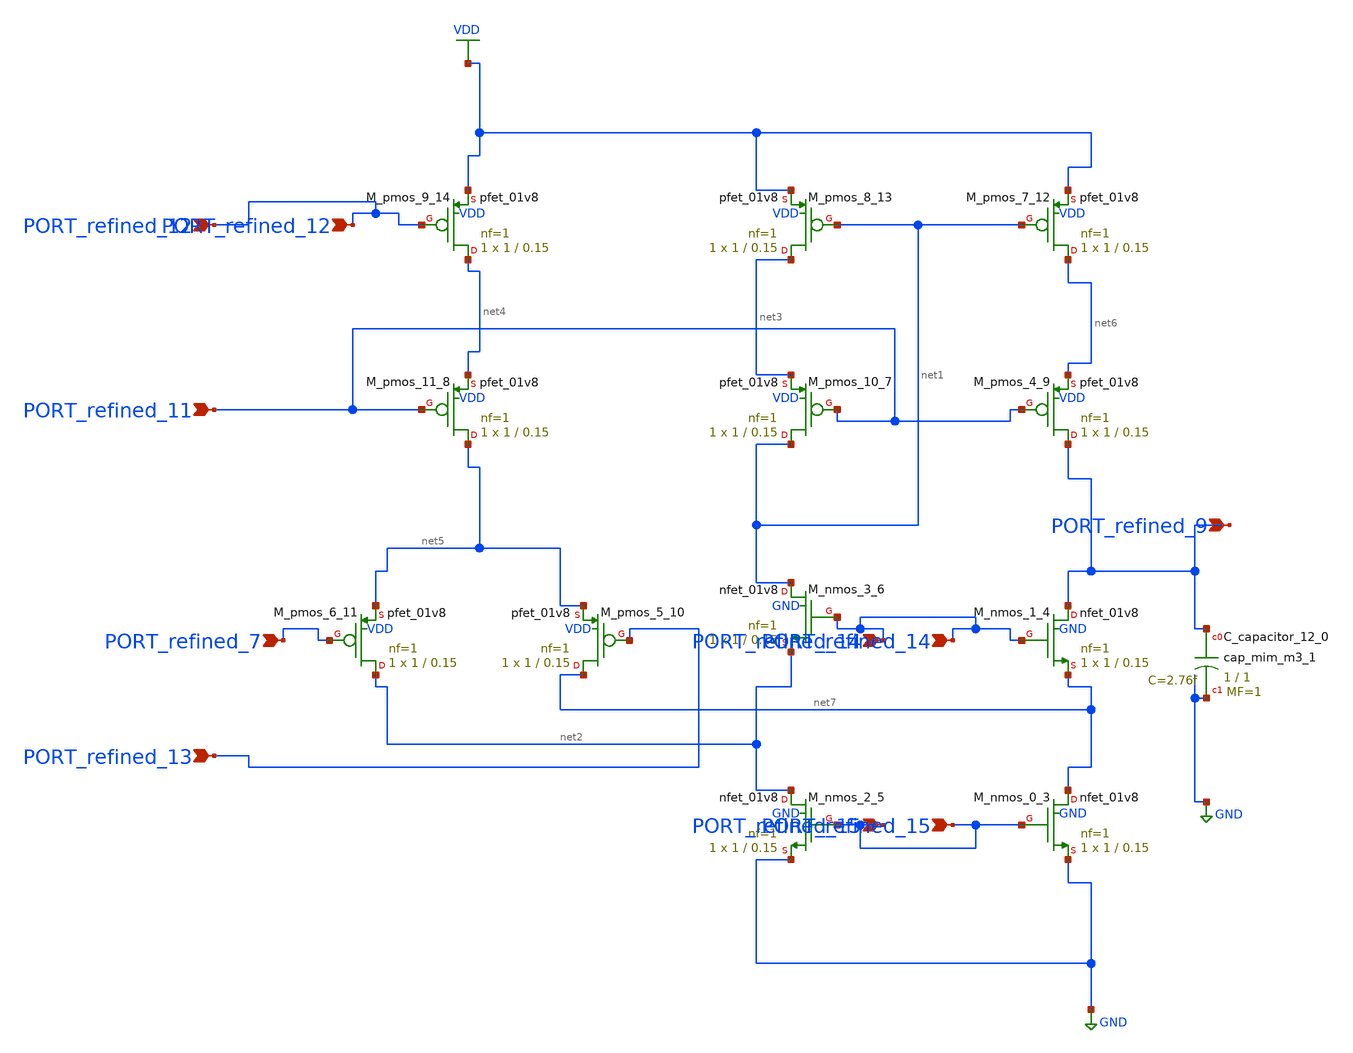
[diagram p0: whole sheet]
** sch_path: schematics/10_24425_ijet_2020_131876_02_002.sch
**.subckt 10_24425_ijet_2020_131876_02_002 PORT_refined_13 PORT_refined_9 PORT_refined_12
*+ PORT_refined_11 PORT_refined_15 PORT_refined_14 PORT_refined_15 PORT_refined_7 PORT_refined_14 PORT_refined_12
*.ipin PORT_refined_13
*.ipin PORT_refined_9
*.ipin PORT_refined_12
*.ipin PORT_refined_11
*.ipin PORT_refined_15
*.ipin PORT_refined_14
*.ipin PORT_refined_15
*.ipin PORT_refined_7
*.ipin PORT_refined_14
*.ipin PORT_refined_12
XC_capacitor_12_0 PORT_refined_9 GND sky130_fd_pr__cap_mim_m3_1 W=1 L=1 MF=1 m=1
XM_nmos_0_3 net7 PORT_refined_15 GND GND sky130_fd_pr__nfet_01v8 L=0.15 W=1 nf=1 ad='int((1 + 1)/2) * 1 / 1 * 0.29'
+ as='int((1 + 2)/2) * 1 / 1 * 0.29' pd='2*int((1 + 1)/2) * (1 / 1 + 0.29)' ps='2*int((1 + 2)/2) * (1 / 1 + 0.29)'
+ nrd='0.29 / 1 ' nrs='0.29 / 1 ' sa=0 sb=0 sd=0 mult=1 m=1
XM_nmos_1_4 PORT_refined_9 PORT_refined_14 net7 GND sky130_fd_pr__nfet_01v8 L=0.15 W=1 nf=1 ad='int((1 + 1)/2) * 1 / 1 * 0.29'
+ as='int((1 + 2)/2) * 1 / 1 * 0.29' pd='2*int((1 + 1)/2) * (1 / 1 + 0.29)' ps='2*int((1 + 2)/2) * (1 / 1 + 0.29)'
+ nrd='0.29 / 1 ' nrs='0.29 / 1 ' sa=0 sb=0 sd=0 mult=1 m=1
XM_nmos_2_5 net2 PORT_refined_15 GND GND sky130_fd_pr__nfet_01v8 L=0.15 W=1 nf=1 ad='int((1 + 1)/2) * 1 / 1 * 0.29'
+ as='int((1 + 2)/2) * 1 / 1 * 0.29' pd='2*int((1 + 1)/2) * (1 / 1 + 0.29)' ps='2*int((1 + 2)/2) * (1 / 1 + 0.29)'
+ nrd='0.29 / 1 ' nrs='0.29 / 1 ' sa=0 sb=0 sd=0 mult=1 m=1
XM_nmos_3_6 net1 PORT_refined_14 net2 GND sky130_fd_pr__nfet_01v8 L=0.15 W=1 nf=1 ad='int((1 + 1)/2) * 1 / 1 * 0.29'
+ as='int((1 + 2)/2) * 1 / 1 * 0.29' pd='2*int((1 + 1)/2) * (1 / 1 + 0.29)' ps='2*int((1 + 2)/2) * (1 / 1 + 0.29)'
+ nrd='0.29 / 1 ' nrs='0.29 / 1 ' sa=0 sb=0 sd=0 mult=1 m=1
XM_pmos_10_7 net1 PORT_refined_11 net3 VDD sky130_fd_pr__pfet_01v8 L=0.15 W=1 nf=1 ad='int((1 + 1)/2) * 1 / 1 * 0.29'
+ as='int((1 + 2)/2) * 1 / 1 * 0.29' pd='2*int((1 + 1)/2) * (1 / 1 + 0.29)' ps='2*int((1 + 2)/2) * (1 / 1 + 0.29)'
+ nrd='0.29 / 1 ' nrs='0.29 / 1 ' sa=0 sb=0 sd=0 mult=1 m=1
XM_pmos_11_8 net5 PORT_refined_11 net4 VDD sky130_fd_pr__pfet_01v8 L=0.15 W=1 nf=1 ad='int((1 + 1)/2) * 1 / 1 * 0.29'
+ as='int((1 + 2)/2) * 1 / 1 * 0.29' pd='2*int((1 + 1)/2) * (1 / 1 + 0.29)' ps='2*int((1 + 2)/2) * (1 / 1 + 0.29)'
+ nrd='0.29 / 1 ' nrs='0.29 / 1 ' sa=0 sb=0 sd=0 mult=1 m=1
XM_pmos_4_9 PORT_refined_9 PORT_refined_11 net6 VDD sky130_fd_pr__pfet_01v8 L=0.15 W=1 nf=1 ad='int((1 + 1)/2) * 1 / 1 * 0.29'
+ as='int((1 + 2)/2) * 1 / 1 * 0.29' pd='2*int((1 + 1)/2) * (1 / 1 + 0.29)' ps='2*int((1 + 2)/2) * (1 / 1 + 0.29)'
+ nrd='0.29 / 1 ' nrs='0.29 / 1 ' sa=0 sb=0 sd=0 mult=1 m=1
XM_pmos_5_10 net7 PORT_refined_13 net5 VDD sky130_fd_pr__pfet_01v8 L=0.15 W=1 nf=1 ad='int((1 + 1)/2) * 1 / 1 * 0.29'
+ as='int((1 + 2)/2) * 1 / 1 * 0.29' pd='2*int((1 + 1)/2) * (1 / 1 + 0.29)' ps='2*int((1 + 2)/2) * (1 / 1 + 0.29)'
+ nrd='0.29 / 1 ' nrs='0.29 / 1 ' sa=0 sb=0 sd=0 mult=1 m=1
XM_pmos_6_11 net2 PORT_refined_7 net5 VDD sky130_fd_pr__pfet_01v8 L=0.15 W=1 nf=1 ad='int((1 + 1)/2) * 1 / 1 * 0.29'
+ as='int((1 + 2)/2) * 1 / 1 * 0.29' pd='2*int((1 + 1)/2) * (1 / 1 + 0.29)' ps='2*int((1 + 2)/2) * (1 / 1 + 0.29)'
+ nrd='0.29 / 1 ' nrs='0.29 / 1 ' sa=0 sb=0 sd=0 mult=1 m=1
XM_pmos_7_12 net6 net1 VDD VDD sky130_fd_pr__pfet_01v8 L=0.15 W=1 nf=1 ad='int((1 + 1)/2) * 1 / 1 * 0.29'
+ as='int((1 + 2)/2) * 1 / 1 * 0.29' pd='2*int((1 + 1)/2) * (1 / 1 + 0.29)' ps='2*int((1 + 2)/2) * (1 / 1 + 0.29)'
+ nrd='0.29 / 1 ' nrs='0.29 / 1 ' sa=0 sb=0 sd=0 mult=1 m=1
XM_pmos_8_13 net3 net1 VDD VDD sky130_fd_pr__pfet_01v8 L=0.15 W=1 nf=1 ad='int((1 + 1)/2) * 1 / 1 * 0.29'
+ as='int((1 + 2)/2) * 1 / 1 * 0.29' pd='2*int((1 + 1)/2) * (1 / 1 + 0.29)' ps='2*int((1 + 2)/2) * (1 / 1 + 0.29)'
+ nrd='0.29 / 1 ' nrs='0.29 / 1 ' sa=0 sb=0 sd=0 mult=1 m=1
XM_pmos_9_14 net4 PORT_refined_12 VDD VDD sky130_fd_pr__pfet_01v8 L=0.15 W=1 nf=1 ad='int((1 + 1)/2) * 1 / 1 * 0.29'
+ as='int((1 + 2)/2) * 1 / 1 * 0.29' pd='2*int((1 + 1)/2) * (1 / 1 + 0.29)' ps='2*int((1 + 2)/2) * (1 / 1 + 0.29)'
+ nrd='0.29 / 1 ' nrs='0.29 / 1 ' sa=0 sb=0 sd=0 mult=1 m=1
**.ends
.GLOBAL GND
.GLOBAL VDD
.end
